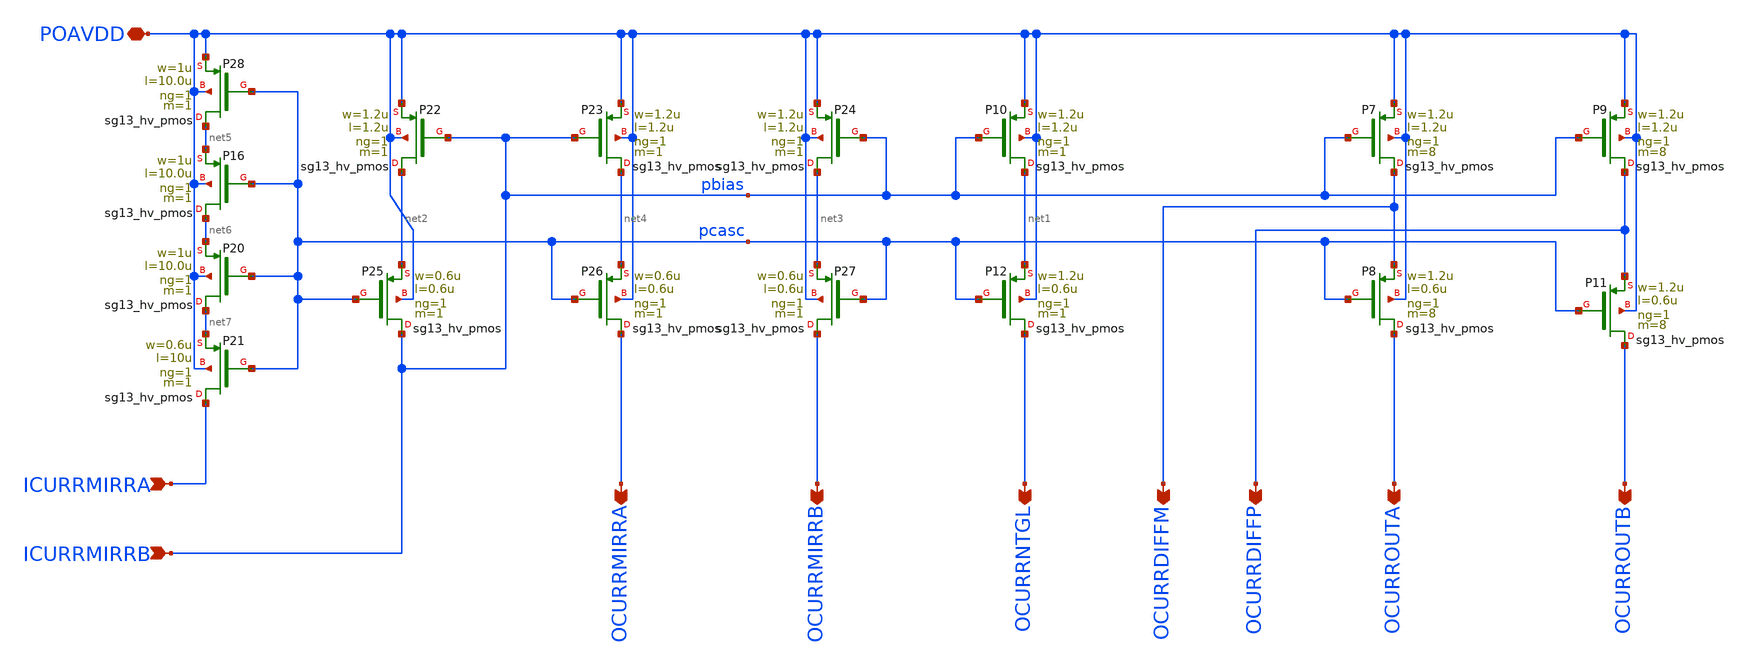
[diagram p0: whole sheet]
** sch_path: xschem/pcasc.sch
**.subckt pcasc POAVDD ICURRMIRRA OCURRMIRRA ICURRMIRRB OCURRMIRRB OCURRNTGL OCURRDIFFM OCURRDIFFP
*+ OCURROUTA OCURROUTB
*.iopin POAVDD
*.ipin ICURRMIRRA
*.opin OCURRMIRRA
*.ipin ICURRMIRRB
*.opin OCURRMIRRB
*.opin OCURRNTGL
*.opin OCURRDIFFM
*.opin OCURRDIFFP
*.opin OCURROUTA
*.opin OCURROUTB
XP10 net1 pbias POAVDD POAVDD sg13_hv_pmos w=1.2u l=1.2u ng=1 m=1 mm_ok=1
XP12 OCURRNTGL pcasc net1 POAVDD sg13_hv_pmos w=1.2u l=0.6u ng=1 m=1 mm_ok=1
XP7 OCURRDIFFM pbias POAVDD POAVDD sg13_hv_pmos w=1.2u l=1.2u ng=1 m=8 mm_ok=1
XP8 OCURROUTA pcasc OCURRDIFFM POAVDD sg13_hv_pmos w=1.2u l=0.6u ng=1 m=8 mm_ok=1
XP9 OCURRDIFFP pbias POAVDD POAVDD sg13_hv_pmos w=1.2u l=1.2u ng=1 m=8 mm_ok=1
XP11 OCURROUTB pcasc OCURRDIFFP POAVDD sg13_hv_pmos w=1.2u l=0.6u ng=1 m=8 mm_ok=1
XP21 ICURRMIRRA pcasc net7 POAVDD sg13_hv_pmos w=0.6u l=10u ng=1 m=1 mm_ok=1
XP20 net7 pcasc net6 POAVDD sg13_hv_pmos w=1u l=10.0u ng=1 m=1 mm_ok=1
XP22 net2 pbias POAVDD POAVDD sg13_hv_pmos w=1.2u l=1.2u ng=1 m=1 mm_ok=1
XP25 pbias pcasc net2 POAVDD sg13_hv_pmos w=0.6u l=0.6u ng=1 m=1 mm_ok=1
XP26 OCURRMIRRA pcasc net4 POAVDD sg13_hv_pmos w=0.6u l=0.6u ng=1 m=1 mm_ok=1
XP23 net4 pbias POAVDD POAVDD sg13_hv_pmos w=1.2u l=1.2u ng=1 m=1 mm_ok=1
XP24 net3 pbias POAVDD POAVDD sg13_hv_pmos w=1.2u l=1.2u ng=1 m=1 mm_ok=1
XP27 OCURRMIRRB pcasc net3 POAVDD sg13_hv_pmos w=0.6u l=0.6u ng=1 m=1 mm_ok=1
XP16 net6 pcasc net5 POAVDD sg13_hv_pmos w=1u l=10.0u ng=1 m=1 mm_ok=1
XP28 net5 pcasc POAVDD POAVDD sg13_hv_pmos w=1u l=10.0u ng=1 m=1 mm_ok=1
**.ends
.end
